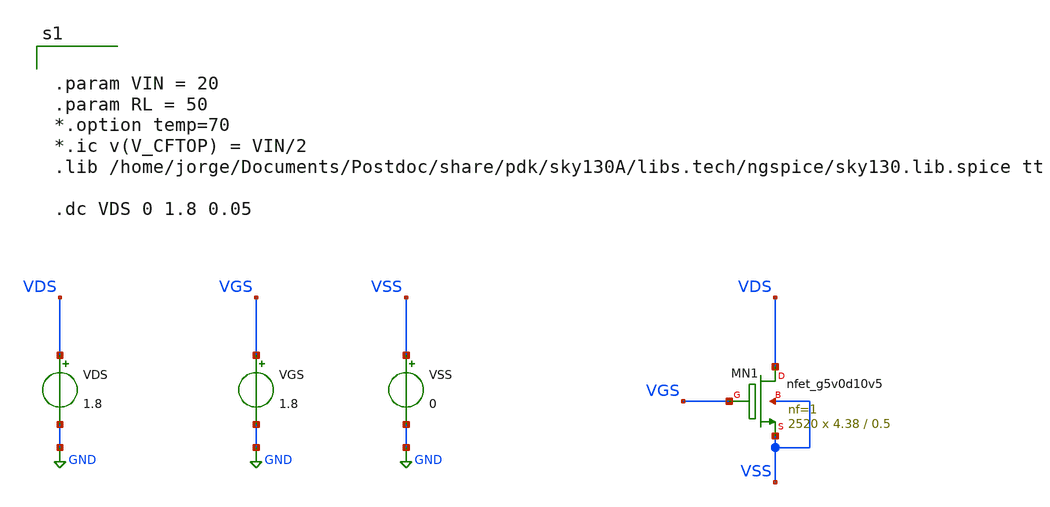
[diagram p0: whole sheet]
** sch_path: xschem/dev_switches/NMOS_allfingers_RONcalc_v1p1_20220614.sch
**.subckt NMOS_allfingers_RONcalc_v1p1_20220614
XMN1 VDS VGS VSS VSS sky130_fd_pr__nfet_g5v0d10v5 L=0.5 W=4.38 nf=1 ad='int((nf+1)/2) * W/nf * 0.29'
+ as='int((nf+2)/2) * W/nf * 0.29' pd='2*int((nf+1)/2) * (W/nf + 0.29)' ps='2*int((nf+2)/2) * (W/nf + 0.29)'
+ nrd='0.29 / W' nrs='0.29 / W' sa=0 sb=0 sd=0 mult=2520 m=2520
VGS VGS GND 1.8
VSS VSS GND 0
VDS VDS GND 1.8
**** begin user architecture code


.param VIN = 20
.param RL = 50
*.option temp=70
*.ic v(V_CFTOP) = VIN/2
.lib /home/jorge/Documents/Postdoc/share/pdk/sky130A/libs.tech/ngspice/sky130.lib.spice tt

.dc VDS 0 1.8 0.05


**** end user architecture code
**.ends
.GLOBAL GND
.end
